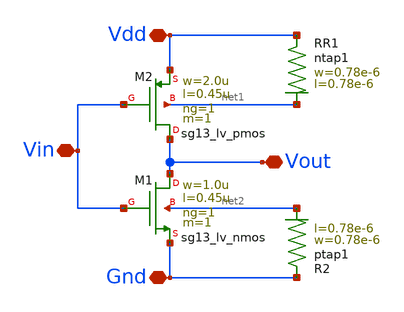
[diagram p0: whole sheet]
** sch_path: utils/PEX_Demo/inverter.sch
**.subckt inverter Vout Vdd Vin Gnd
*.iopin Vout
*.iopin Vdd
*.iopin Vin
*.iopin Gnd
XM1 Vout Vin Gnd net2 sg13_lv_nmos w=1.0u l=0.45u ng=1 m=1 mm_ok=1
XM2 Vout Vin Vdd net1 sg13_lv_pmos w=2.0u l=0.45u ng=1 m=1 mm_ok=1
XR1 Vdd net1 ntap1 R=262.8 w=0.78e-6 l=0.78e-6
XR2 Gnd net2 ptap1 R=262.8 w=0.78e-6 l=0.78e-6
**.ends
.end
